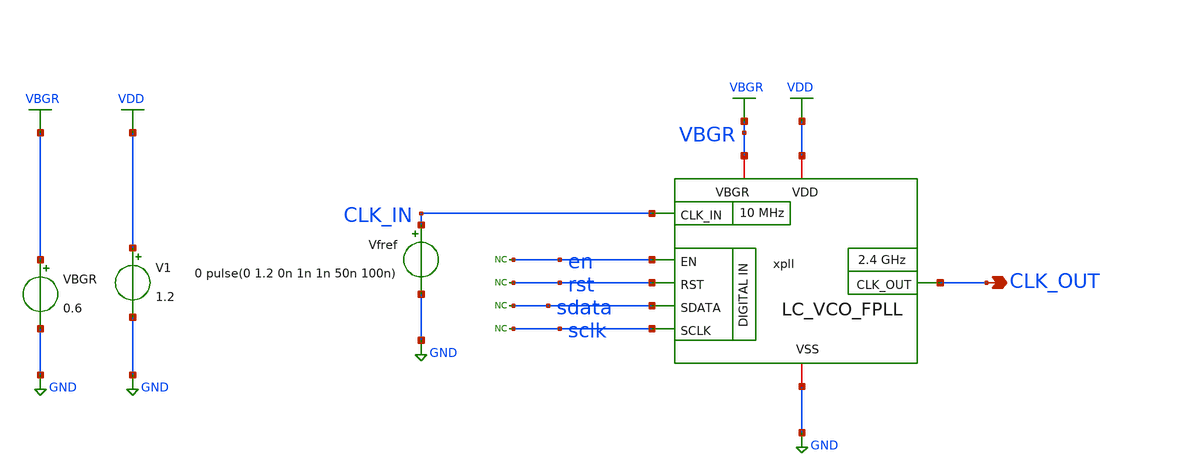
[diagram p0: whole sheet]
** sch_path: xschem/top-pll/LC_VCO_FPLL_tb.sch
**.subckt LC_VCO_FPLL_tb CLK_OUT
*.opin CLK_OUT
V1 VDD GND 1.2
Vfref CLK_IN GND 0 pulse(0 1.2 0n 1n 1n 50n 100n)
VBGR VBGR GND 0.6
xpll VBGR CLK_IN VDD CLK_OUT GND en rst sdata sclk LC_VCO_FPLL
* noconn en
* noconn rst
* noconn sdata
* noconn sclk
**** begin user architecture code



*****************************************************
* PLL + DSM Frequency Divider Testbench (Optimized)
*****************************************************

.option temp=27
.param VDD=1.2
.option rshunt = 1.0e12

* ==============================
* Include Models & Stimuli
* ==============================
.include 4nH_INDUCTOR.spice
.include ../simulations/stimuli_test.cir

* ==============================
* Simulation Options (Optimized for Speed & Stability)
* ==============================
* gear method improves stability for long oscillator runs
* reltol=1e-3 prevents the simulator from bogging down on microscopic errors
.options reltol=1e-3 abstol=1e-9 vntol=1e-6 method=gear

.control
  * CRITICAL: Save ONLY essential low-frequency signals.
  save xpll.vctrl xpll.up xpll.dn xpll.clk_fb clk_out clk_in vbgr xpll.vcp xpll.x4.outp sdata sclk
+ en rst


  * 20p defines the step to resolve the 2.4 GHz edges without forcing a maxstep.
  tran 10p 100u

  remzerovec
  write tb_LC_VCO_FPLL_100u.raw
.endc






.lib cornerMOSlv.lib mos_tt
.lib cornerMOShv.lib mos_tt
.lib cornerHBT.lib hbt_typ
.lib cornerRES.lib res_typ
.lib cornerCAP.lib cap_typ
.include /foss/pdks/ihp-sg13g2/libs.ref/sg13g2_stdcell/spice/sg13g2_stdcell.spice
*.include /opt/pdks/ihp-sg13g2/libs.ref/sg13g2_stdcell/spice/sg13g2_stdcell.spice
.global VDD GND




**** end user architecture code
**.ends
.GLOBAL GND
.GLOBAL VDD
.GLOBAL VBGR
.end
